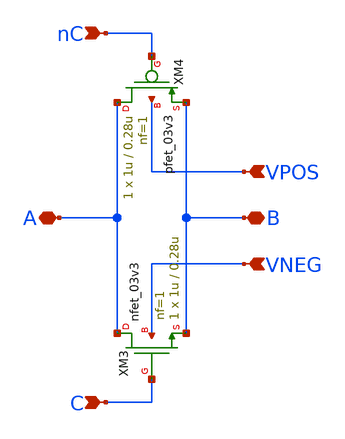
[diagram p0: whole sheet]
** sch_path: xschem/blocks/transmission_gate/transmission_gate.sch
**.subckt transmission_gate A B C nC VPOS VNEG
*.iopin A
*.iopin B
*.ipin C
*.ipin nC
*.ipin VPOS
*.ipin VNEG
XM3 A C B VNEG nfet_03v3 L=0.28u W=1u nf=1 ad='int((nf+1)/2) * W/nf * 0.18u' as='int((nf+2)/2) * W/nf * 0.18u'
+ pd='2*int((nf+1)/2) * (W/nf + 0.18u)' ps='2*int((nf+2)/2) * (W/nf + 0.18u)' nrd='0.18u / W' nrs='0.18u / W'
+ sa=0 sb=0 sd=0 m=1
XM4 A nC B VPOS pfet_03v3 L=0.28u W=1u nf=1 ad='int((nf+1)/2) * W/nf * 0.18u' as='int((nf+2)/2) * W/nf * 0.18u'
+ pd='2*int((nf+1)/2) * (W/nf + 0.18u)' ps='2*int((nf+2)/2) * (W/nf + 0.18u)' nrd='0.18u / W' nrs='0.18u / W'
+ sa=0 sb=0 sd=0 m=1
**.ends
.end
